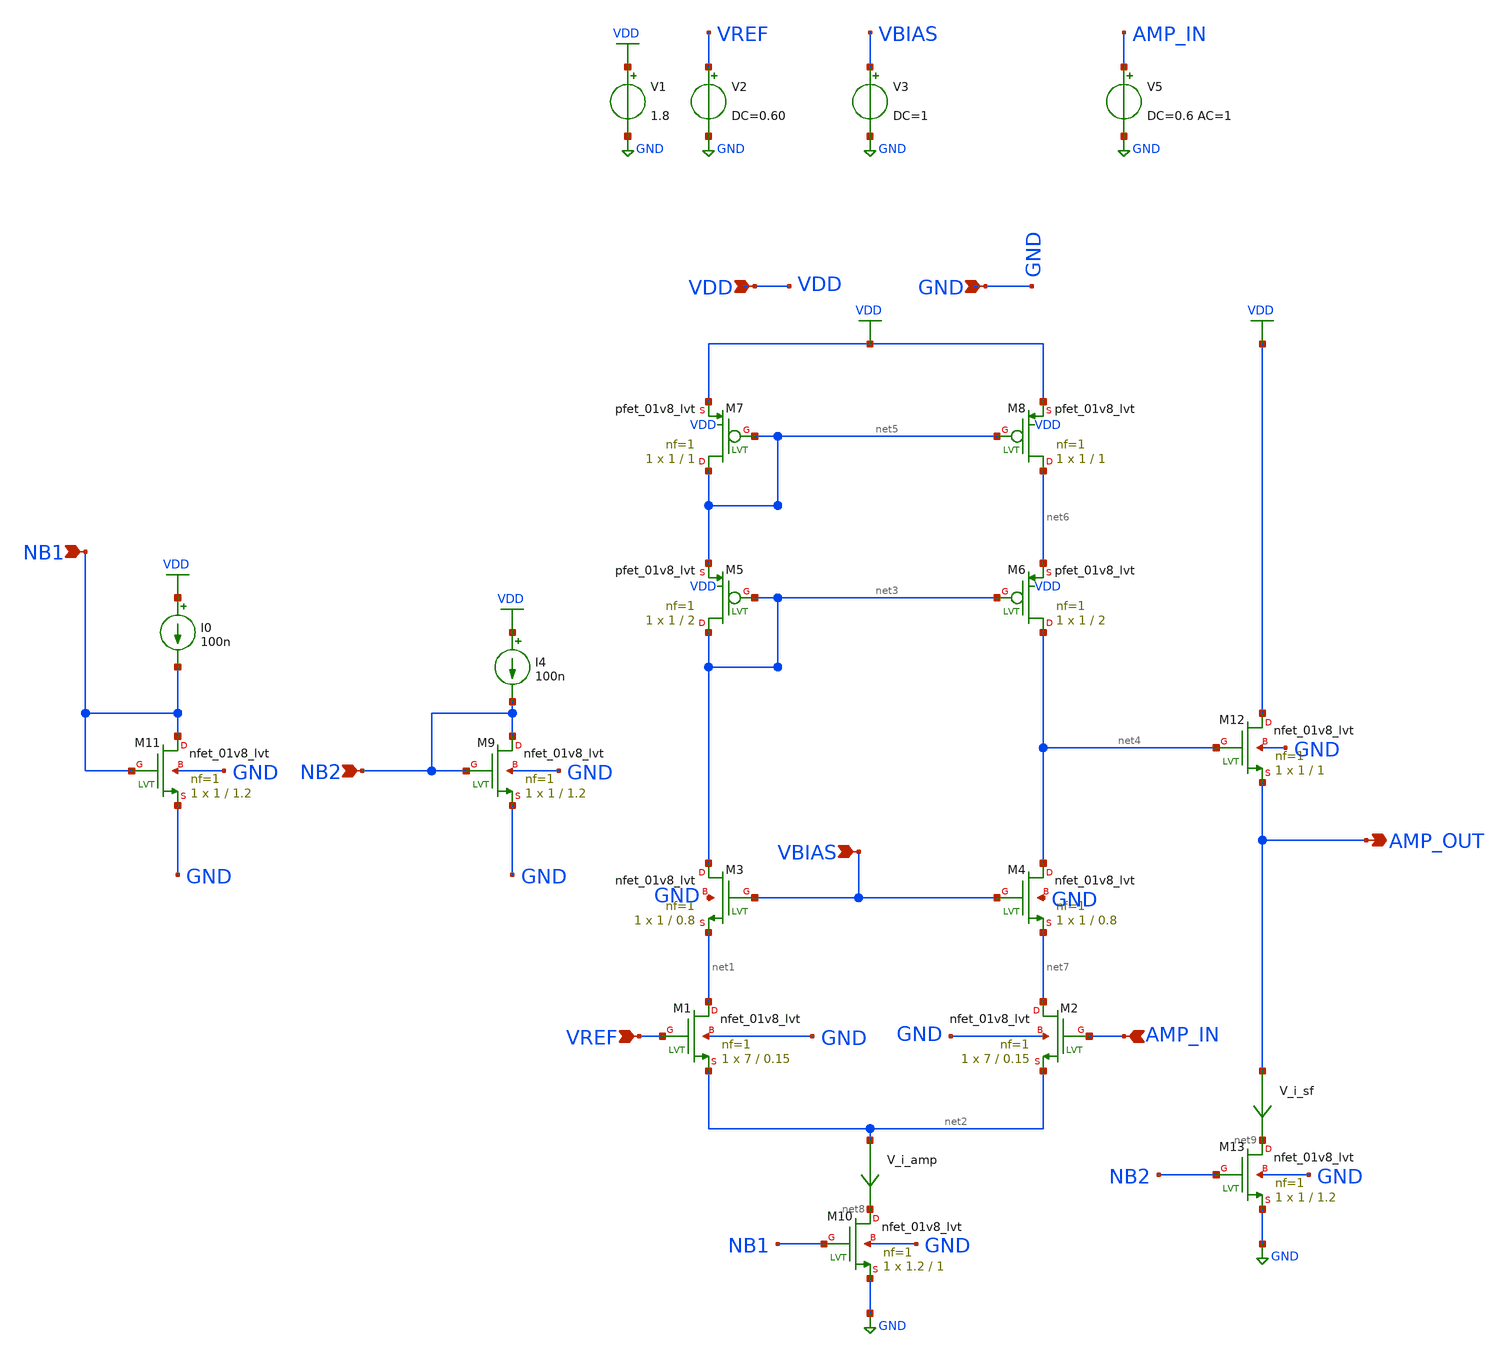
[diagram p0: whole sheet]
** sch_path: xschem/testbench/nmos_cs.sch
**.subckt nmos_cs VREF AMP_IN VBIAS VDD GND AMP_OUT NB1 NB2
*.ipin VREF
*.ipin AMP_IN
*.ipin VBIAS
*.ipin VDD
*.ipin GND
*.opin AMP_OUT
*.ipin NB1
*.ipin NB2
V1 VDD GND 1.8
V2 VREF GND DC=0.60
V3 VBIAS GND DC=1
XM5 net3 net3 net5 VDD sky130_fd_pr__pfet_01v8_lvt L=2 W=1 nf=1 ad='int((nf+1)/2) * W/nf * 0.29' as='int((nf+2)/2) * W/nf * 0.29'
+ pd='2*int((nf+1)/2) * (W/nf + 0.29)' ps='2*int((nf+2)/2) * (W/nf + 0.29)' nrd='0.29 / W' nrs='0.29 / W'
+ sa=0 sb=0 sd=0 mult=1 m=1
XM8 net6 net5 VDD VDD sky130_fd_pr__pfet_01v8_lvt L=1 W=1 nf=1 ad='int((nf+1)/2) * W/nf * 0.29' as='int((nf+2)/2) * W/nf * 0.29'
+ pd='2*int((nf+1)/2) * (W/nf + 0.29)' ps='2*int((nf+2)/2) * (W/nf + 0.29)' nrd='0.29 / W' nrs='0.29 / W'
+ sa=0 sb=0 sd=0 mult=1 m=1
XM7 net5 net5 VDD VDD sky130_fd_pr__pfet_01v8_lvt L=1 W=1 nf=1 ad='int((nf+1)/2) * W/nf * 0.29' as='int((nf+2)/2) * W/nf * 0.29'
+ pd='2*int((nf+1)/2) * (W/nf + 0.29)' ps='2*int((nf+2)/2) * (W/nf + 0.29)' nrd='0.29 / W' nrs='0.29 / W'
+ sa=0 sb=0 sd=0 mult=1 m=1
XM10 net8 NB1 GND GND sky130_fd_pr__nfet_01v8_lvt L=1 W=1.2 nf=1 ad='int((nf+1)/2) * W/nf * 0.29' as='int((nf+2)/2) * W/nf * 0.29'
+ pd='2*int((nf+1)/2) * (W/nf + 0.29)' ps='2*int((nf+2)/2) * (W/nf + 0.29)' nrd='0.29 / W' nrs='0.29 / W'
+ sa=0 sb=0 sd=0 mult=1 m=1
XM1 net1 VREF net2 GND sky130_fd_pr__nfet_01v8_lvt L=0.15 W=7 nf=1 ad='int((nf+1)/2) * W/nf * 0.29' as='int((nf+2)/2) * W/nf * 0.29'
+ pd='2*int((nf+1)/2) * (W/nf + 0.29)' ps='2*int((nf+2)/2) * (W/nf + 0.29)' nrd='0.29 / W' nrs='0.29 / W'
+ sa=0 sb=0 sd=0 mult=1 m=1
XM6 net4 net3 net6 VDD sky130_fd_pr__pfet_01v8_lvt L=2 W=1 nf=1 ad='int((nf+1)/2) * W/nf * 0.29' as='int((nf+2)/2) * W/nf * 0.29'
+ pd='2*int((nf+1)/2) * (W/nf + 0.29)' ps='2*int((nf+2)/2) * (W/nf + 0.29)' nrd='0.29 / W' nrs='0.29 / W'
+ sa=0 sb=0 sd=0 mult=1 m=1
XM3 net3 VBIAS net1 GND sky130_fd_pr__nfet_01v8_lvt L=0.8 W=1 nf=1 ad='int((nf+1)/2) * W/nf * 0.29' as='int((nf+2)/2) * W/nf * 0.29'
+ pd='2*int((nf+1)/2) * (W/nf + 0.29)' ps='2*int((nf+2)/2) * (W/nf + 0.29)' nrd='0.29 / W' nrs='0.29 / W'
+ sa=0 sb=0 sd=0 mult=1 m=1
XM2 net7 AMP_IN net2 GND sky130_fd_pr__nfet_01v8_lvt L=0.15 W=7 nf=1 ad='int((nf+1)/2) * W/nf * 0.29'
+ as='int((nf+2)/2) * W/nf * 0.29' pd='2*int((nf+1)/2) * (W/nf + 0.29)' ps='2*int((nf+2)/2) * (W/nf + 0.29)'
+ nrd='0.29 / W' nrs='0.29 / W' sa=0 sb=0 sd=0 mult=1 m=1
XM4 net4 VBIAS net7 GND sky130_fd_pr__nfet_01v8_lvt L=0.8 W=1 nf=1 ad='int((nf+1)/2) * W/nf * 0.29' as='int((nf+2)/2) * W/nf * 0.29'
+ pd='2*int((nf+1)/2) * (W/nf + 0.29)' ps='2*int((nf+2)/2) * (W/nf + 0.29)' nrd='0.29 / W' nrs='0.29 / W'
+ sa=0 sb=0 sd=0 mult=1 m=1
XM12 VDD net4 AMP_OUT GND sky130_fd_pr__nfet_01v8_lvt L=1 W=1 nf=1 ad='int((nf+1)/2) * W/nf * 0.29' as='int((nf+2)/2) * W/nf * 0.29'
+ pd='2*int((nf+1)/2) * (W/nf + 0.29)' ps='2*int((nf+2)/2) * (W/nf + 0.29)' nrd='0.29 / W' nrs='0.29 / W'
+ sa=0 sb=0 sd=0 mult=1 m=1
XM13 net9 NB2 GND GND sky130_fd_pr__nfet_01v8_lvt L=1.2 W=1 nf=1 ad='int((nf+1)/2) * W/nf * 0.29' as='int((nf+2)/2) * W/nf * 0.29'
+ pd='2*int((nf+1)/2) * (W/nf + 0.29)' ps='2*int((nf+2)/2) * (W/nf + 0.29)' nrd='0.29 / W' nrs='0.29 / W'
+ sa=0 sb=0 sd=0 mult=1 m=1
XM11 NB1 NB1 GND GND sky130_fd_pr__nfet_01v8_lvt L=1.2 W=1 nf=1 ad='int((nf+1)/2) * W/nf * 0.29' as='int((nf+2)/2) * W/nf * 0.29'
+ pd='2*int((nf+1)/2) * (W/nf + 0.29)' ps='2*int((nf+2)/2) * (W/nf + 0.29)' nrd='0.29 / W' nrs='0.29 / W'
+ sa=0 sb=0 sd=0 mult=1 m=1
I0 VDD NB1 100n
I4 VDD NB2 100n
XM9 NB2 NB2 GND GND sky130_fd_pr__nfet_01v8_lvt L=1.2 W=1 nf=1 ad='int((nf+1)/2) * W/nf * 0.29' as='int((nf+2)/2) * W/nf * 0.29'
+ pd='2*int((nf+1)/2) * (W/nf + 0.29)' ps='2*int((nf+2)/2) * (W/nf + 0.29)' nrd='0.29 / W' nrs='0.29 / W'
+ sa=0 sb=0 sd=0 mult=1 m=1
V5 AMP_IN GND DC=0.6 AC=1
V_i_amp net2 net8 0
.save i(v_i_amp)
V_i_sf AMP_OUT net9 0
.save i(v_i_sf)
**** begin user architecture code

** opencircuitdesign pdks install
.lib $::SKYWATER_MODELS/sky130.lib.spice tt


**** end user architecture code
**.ends
.GLOBAL GND
.GLOBAL VDD
**** begin user architecture code


.options gmin=0.0000000000000000000001
*.options savecurrents

.control
save all

*DC V5 0.4 1 0.0001
*plot v(amp_out)
*plot deriv(v(amp_out))

*op

ac dec 10 1 100G
plot vdb(AMP_OUT)


*noise v(PIX_OUT) V8 dec 10 1 1Meg
*setplot noise2
*print onoise_total

*noise v(PIX_OUT) V8 dec 10 1 1Meg
*setplot noise2
*print onoise_total
.endc


**** end user architecture code
.end
